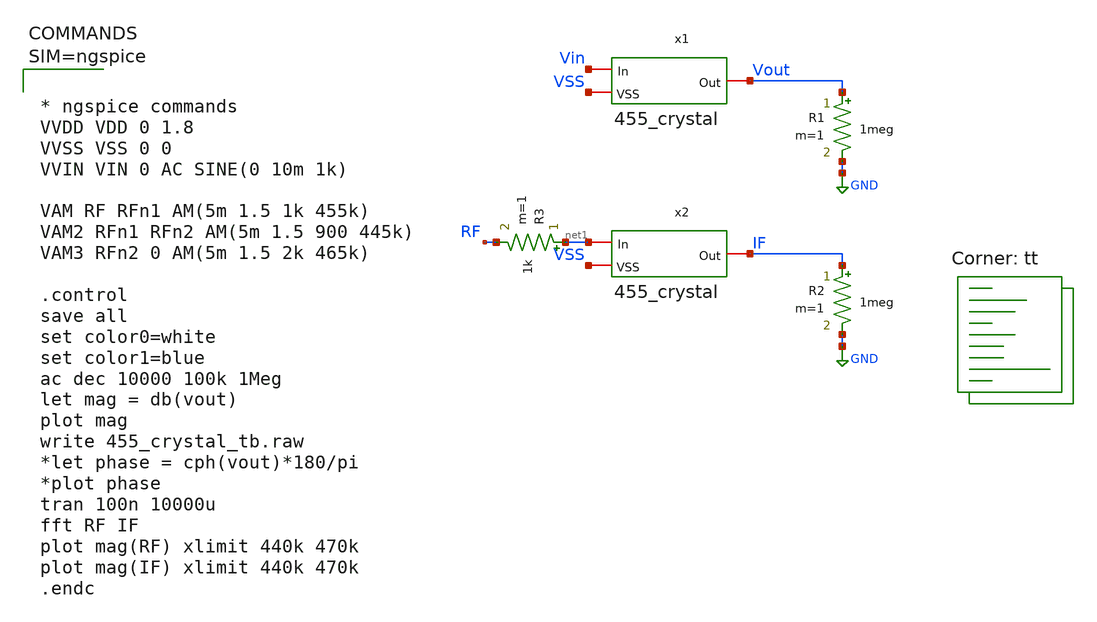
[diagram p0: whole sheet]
** sch_path: Project/xschem/455_crystal_tb.sch
**.subckt 455_crystal_tb
x1 Vin Vout VSS 455_crystal
R1 Vout GND 1meg m=1
x2 net1 IF VSS 455_crystal
R2 IF GND 1meg m=1
R3 net1 RF 1k m=1
**** begin user architecture code
.lib $::SKYWATER_MODELS/sky130.lib.spice tt



* ngspice commands
VVDD VDD 0 1.8
VVSS VSS 0 0
VVIN VIN 0 AC SINE(0 10m 1k)

VAM RF RFn1 AM(5m 1.5 1k 455k)
VAM2 RFn1 RFn2 AM(5m 1.5 900 445k)
VAM3 RFn2 0 AM(5m 1.5 2k 465k)

.control
save all
set color0=white
set color1=blue
ac dec 10000 100k 1Meg
let mag = db(vout)
plot mag
write 455_crystal_tb.raw
*let phase = cph(vout)*180/pi
*plot phase
tran 100n 10000u
fft RF IF
plot mag(RF) xlimit 440k 470k
plot mag(IF) xlimit 440k 470k
.endc



**** end user architecture code
**.ends
.GLOBAL GND
.end
